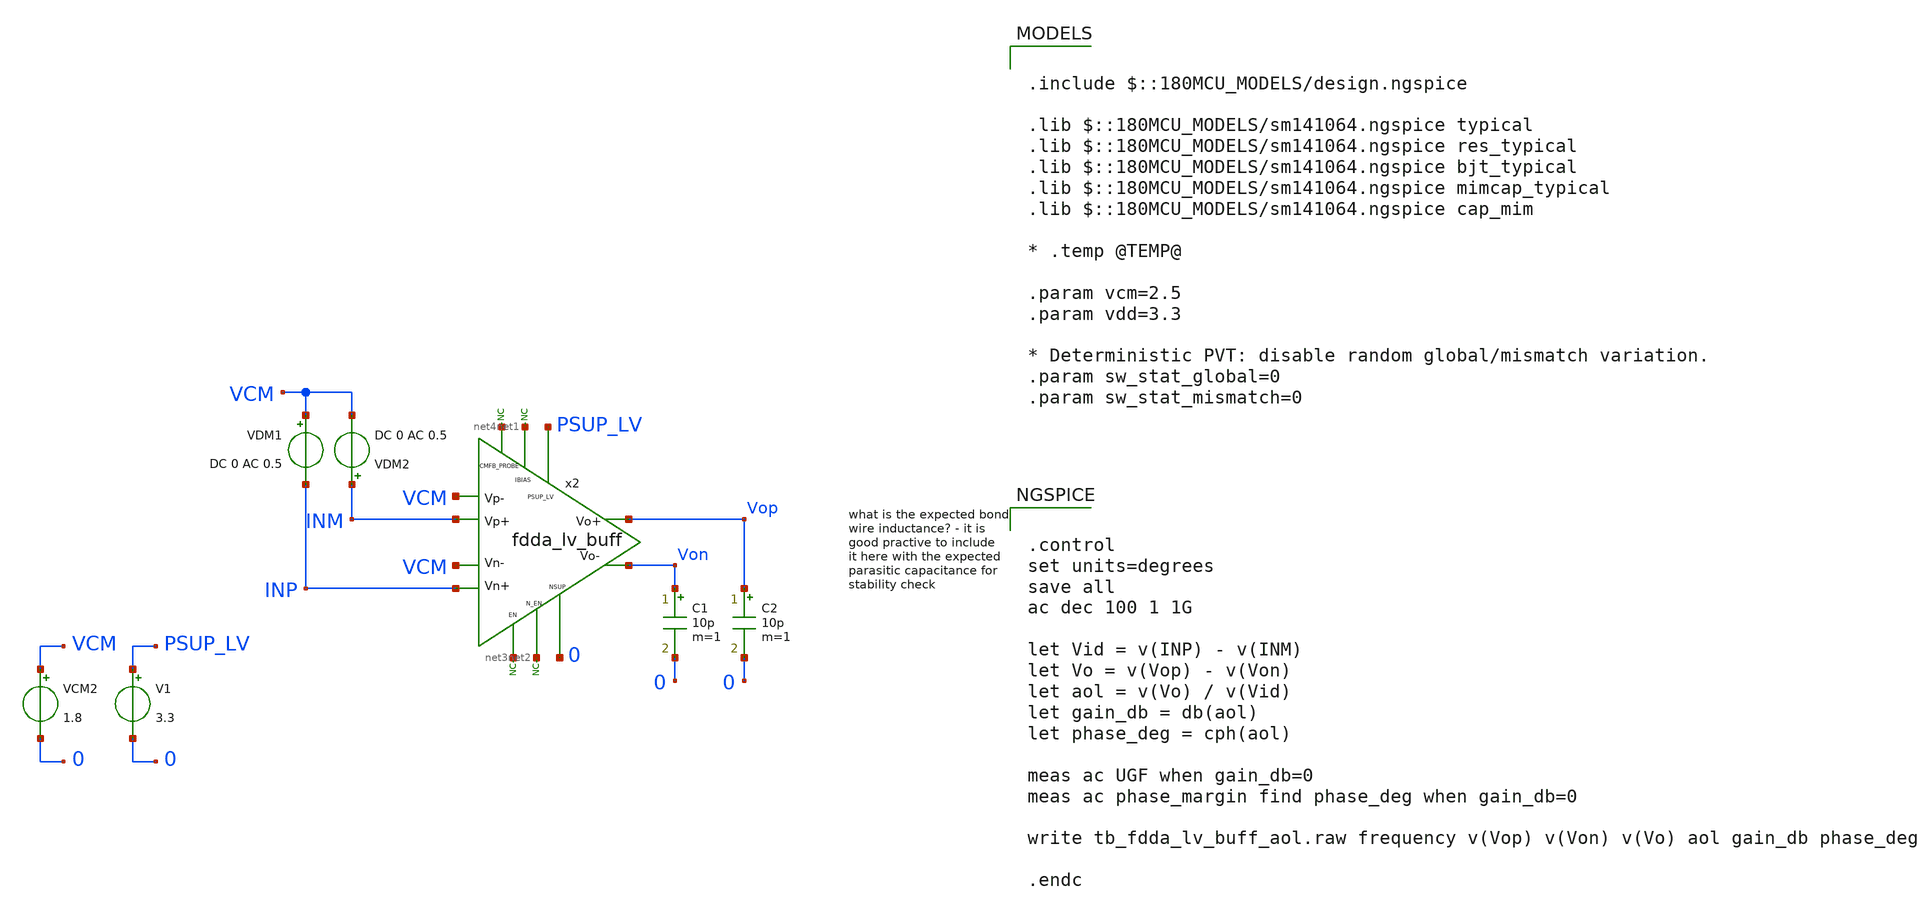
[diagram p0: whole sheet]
** sch_path: xschem/blocks/fdda_lv_buff/tb_fdda_lv_buff_aol.sch
**.subckt tb_fdda_lv_buff_aol
C1 Von 0 10p m=1
x2 PSUP_LV VCM VCM INP INM Vop Von net1 net2 net3 0 net4 fdda_lv_buff
* noconn #net1
* noconn #net3
* noconn #net2
V1 PSUP_LV 0 3.3
C2 Vop 0 10p m=1
VCM2 VCM 0 1.8
VDM2 INM VCM DC 0 AC 0.5
VDM1 VCM INP DC 0 AC 0.5
* noconn #net4
**** begin user architecture code

.include $::180MCU_MODELS/design.ngspice

.lib $::180MCU_MODELS/sm141064.ngspice typical
.lib $::180MCU_MODELS/sm141064.ngspice res_typical
.lib $::180MCU_MODELS/sm141064.ngspice bjt_typical
.lib $::180MCU_MODELS/sm141064.ngspice mimcap_typical
.lib $::180MCU_MODELS/sm141064.ngspice cap_mim

* .temp @TEMP@

.param vcm=2.5
.param vdd=3.3

* Deterministic PVT: disable random global/mismatch variation.
.param sw_stat_global=0
.param sw_stat_mismatch=0



.control
set units=degrees
save all
ac dec 100 1 1G

let Vid = v(INP) - v(INM)
let Vo = v(Vop) - v(Von)
let aol = v(Vo) / v(Vid)
let gain_db = db(aol)
let phase_deg = cph(aol)

meas ac UGF when gain_db=0
meas ac phase_margin find phase_deg when gain_db=0

write tb_fdda_lv_buff_aol.raw frequency v(Vop) v(Von) v(Vo) aol gain_db phase_deg

.endc


**** end user architecture code
**.ends
.end
